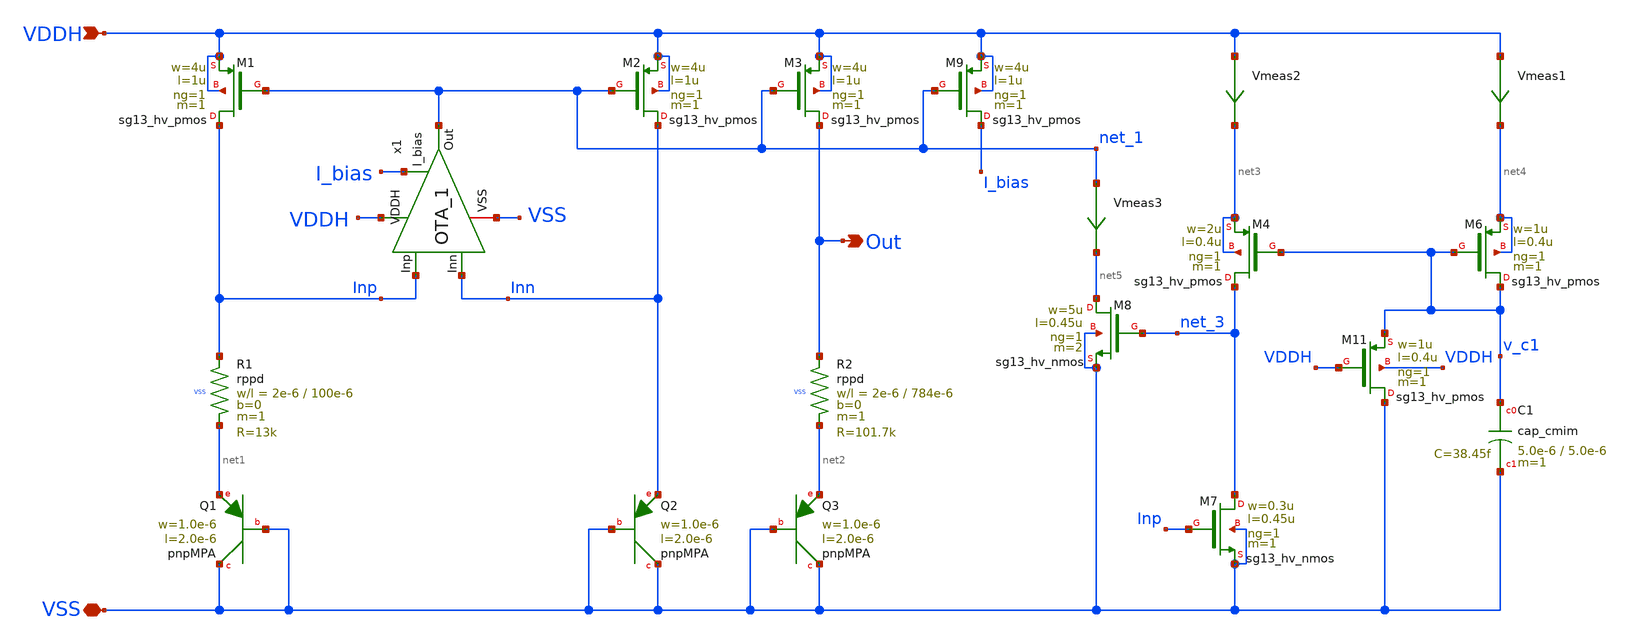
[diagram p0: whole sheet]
** sch_path: sar_adc/xschem/blocks/bandgap/1.2v_bandgap.sch
**.subckt 1.2v_bandgap VSS VDDH Out
*.iopin VSS
*.ipin VDDH
*.opin Out
XM1 Inp net_1 VDDH VDDH sg13_hv_pmos w=4u l=1u ng=1 m=1 mm_ok=1
x1 VDDH Inp Inn net_1 I_bias VSS OTA_1
XM2 Inn net_1 VDDH VDDH sg13_hv_pmos w=4u l=1u ng=1 m=1 mm_ok=1
XR1 Inp net1 VSS rppd w=2e-6 l=100e-6 m=1 b=0 mm_ok=1
XQ1 VSS VSS net1 pnpMPA a=2p p=6u m=8
XQ2 VSS VSS Inn pnpMPA a=2p p=6u m=1
XM3 Out net_1 VDDH VDDH sg13_hv_pmos w=4u l=1u ng=1 m=1 mm_ok=1
XQ3 VSS VSS net2 pnpMPA a=2p p=6u m=1
XR2 Out net2 VSS rppd w=2e-6 l=784e-6 m=1 b=0 mm_ok=1
XM9 I_bias net_1 VDDH VDDH sg13_hv_pmos w=4u l=1u ng=1 m=1 mm_ok=1
XM4 net_3 v_c1 net3 net3 sg13_hv_pmos w=2u l=0.4u ng=1 m=1 mm_ok=1
XM6 v_c1 v_c1 net4 net4 sg13_hv_pmos w=1u l=0.4u ng=1 m=1 mm_ok=1
XM7 net_3 Inp VSS VSS sg13_hv_nmos w=0.3u l=0.45u ng=1 m=1 mm_ok=1
XM8 net5 net_3 VSS VSS sg13_hv_nmos w=5u l=0.45u ng=1 m=2 mm_ok=1
XC1 v_c1 VSS cap_cmim w=5.0e-6 l=5.0e-6 m=1 mm_ok=1
XM11 VSS VDDH v_c1 VDDH sg13_hv_pmos w=1u l=0.4u ng=1 m=1 mm_ok=1
Vmeas2 VDDH net3 0
.save i(vmeas2)
Vmeas3 net_1 net5 0
.save i(vmeas3)
Vmeas1 VDDH net4 0
.save i(vmeas1)
**.ends
.end
